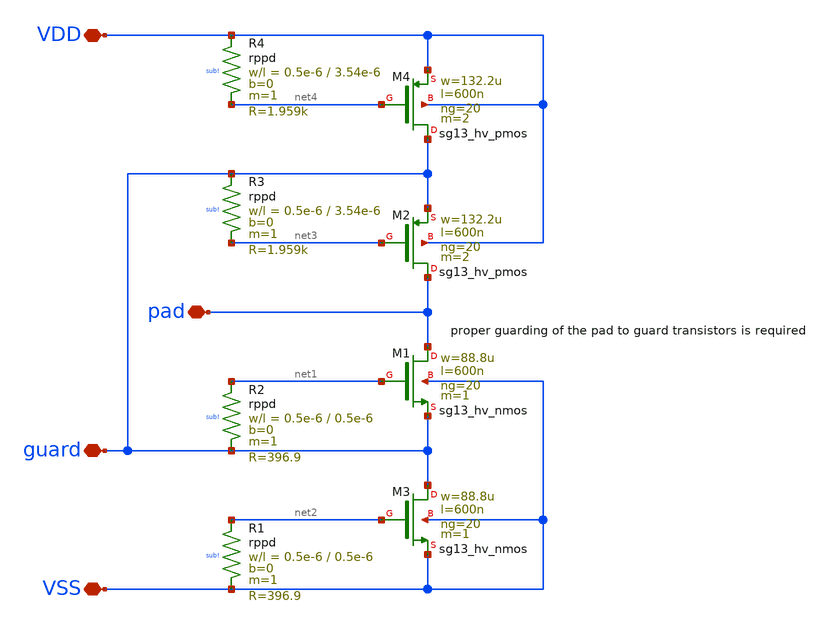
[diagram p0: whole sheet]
** sch_path: trident_test_structures/design_data/xschem/IOPadAnalogGuardLayer/clamps_guard_layer_x1.sch
**.subckt clamps_guard_layer_x1 VSS VDD pad guard
*.iopin VSS
*.iopin VDD
*.iopin pad
*.iopin guard
XM1 pad net1 guard VSS sg13_hv_nmos w=88.8u l=600n ng=20 m=1 mm_ok=1
XM3 guard net2 VSS VSS sg13_hv_nmos w=88.8u l=600n ng=20 m=1 mm_ok=1
XM2 pad net3 guard VDD sg13_hv_pmos w=132.2u l=600n ng=20 m=2 mm_ok=1
XR1 net2 VSS sub! rppd w=0.5e-6 l=0.5e-6 m=1 b=0 mm_ok=1
XR2 net1 guard sub! rppd w=0.5e-6 l=0.5e-6 m=1 b=0 mm_ok=1
XR3 guard net3 sub! rppd w=0.5e-6 l=3.54e-6 m=1 b=0 mm_ok=1
XR4 VDD net4 sub! rppd w=0.5e-6 l=3.54e-6 m=1 b=0 mm_ok=1
XM4 guard net4 VDD VDD sg13_hv_pmos w=132.2u l=600n ng=20 m=2 mm_ok=1
**.ends
.end
